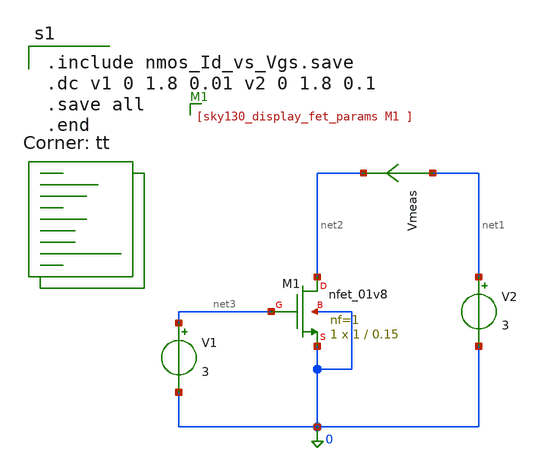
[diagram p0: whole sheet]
** sch_path: Id vs Vgs/Schematic /nmos_dc_sweep.sch
**.subckt nmos_dc_sweep
XM1 net2 net3 0 0 sky130_fd_pr__nfet_01v8 L=0.15 W=1 nf=1 ad='int((1 + 1)/2) * 1 / 1 * 0.29' as='int((1 + 2)/2) * 1 / 1 * 0.29'
+ pd='2*int((1 + 1)/2) * (1 / 1 + 0.29)' ps='2*int((1 + 2)/2) * (1 / 1 + 0.29)' nrd='0.29 / 1 ' nrs='0.29 / 1 '
+ sa=0 sb=0 sd=0 mult=1 m=1
V1 net3 0 3
V2 net1 0 3
Vmeas net1 net2 0
.save i(vmeas)
**** begin user architecture code
.lib $::SKYWATER_MODELS/sky130.lib.spice tt

.include nmos_Id_vs_Vgs.save
.dc v1 0 1.8 0.01 v2 0 1.8 0.1
.save all
.end


**** end user architecture code
**.ends
.end
